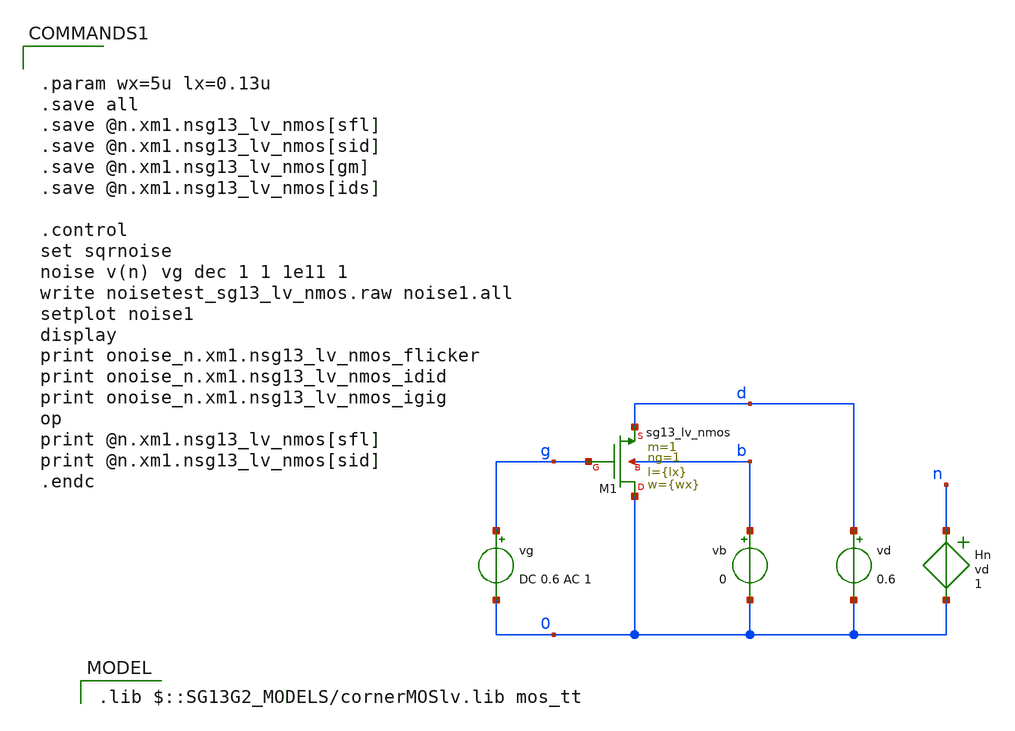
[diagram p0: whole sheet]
** sch_path: model/calculations/ihp-sg13g2_lookup/noisetest_sg13_lv_nmos.sch
**.subckt noisetest_sg13_lv_nmos
vg g 0 DC 0.6 AC 1
vd d 0 0.6
vb b 0 0
Hn n 0 vd 1
XM1 0 g d b sg13_lv_nmos w={wx} l={lx} ng=1 m=1 mm_ok=1
**** begin user architecture code


.param wx=5u lx=0.13u
.save all
.save @n.xm1.nsg13_lv_nmos[sfl]
.save @n.xm1.nsg13_lv_nmos[sid]
.save @n.xm1.nsg13_lv_nmos[gm]
.save @n.xm1.nsg13_lv_nmos[ids]

.control
set sqrnoise
noise v(n) vg dec 1 1 1e11 1
write noisetest_sg13_lv_nmos.raw noise1.all
setplot noise1
display
print onoise_n.xm1.nsg13_lv_nmos_flicker
print onoise_n.xm1.nsg13_lv_nmos_idid
print onoise_n.xm1.nsg13_lv_nmos_igig
op
print @n.xm1.nsg13_lv_nmos[sfl]
print @n.xm1.nsg13_lv_nmos[sid]
.endc


 .lib $::SG13G2_MODELS/cornerMOSlv.lib mos_tt
**** end user architecture code
**.ends
.end
